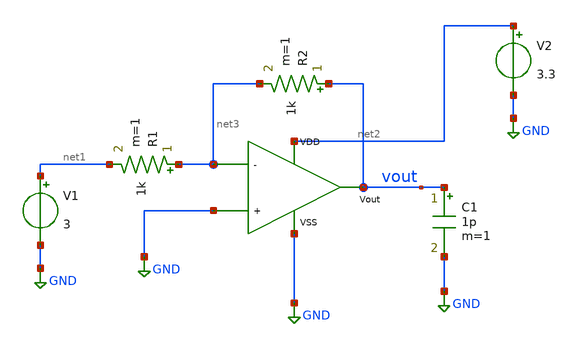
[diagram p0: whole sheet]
** sch_path: xschem/ota_miller/prueba.sch
**.subckt prueba
x1 net2 vout GND net3 GND ota_n_in
R1 net3 net1 1k m=1
R2 vout net3 1k m=1
V1 net1 GND 3
V2 net2 GND 3.3
C1 vout GND 1p m=1
**** begin user architecture code


.control
save all
* Coloracion de graficas
set color0=white
set color1=black
set color2=blue
set color3=red
set xbrushwidth=2

* 1. Convertir V1 a onda senoidal: Offset = 0V, Amplitud = 0.5V, Frecuencia = 1kHz
alter V1 sin(0 0.5 1k)

* 2. Simular 5 ms con paso de 1 us (5 ciclos de 1 kHz)
tran 1u 5m

* 3. Graficar la señal de salida Vout
plot v(Vout) title 'Respuesta Transitoria Inversor OTA 5T' xlabel 'Tiempo (s)' ylabel 'Voltaje (V)'
.endc




.include /home/ringosinye/eda/pdks/gf180mcuD/libs.tech/ngspice/design.ngspice
.lib /home/ringosinye/eda/pdks/gf180mcuD/libs.tech/ngspice/sm141064.ngspice typical
.param sw_stat_mismatch = 0


**** end user architecture code
**.ends

* expanding   symbol:  ota_n_in.sym # of pins=5
** sym_path: xschem/ota_miller/ota_n_in.sym
** sch_path: xschem/ota_miller/ota_n_in.sch
.subckt ota_n_in VDD Vout + - VSS
*.opin Vout
*.ipin VSS
*.ipin VDD
*.ipin +
*.ipin -
XM1 net2 + net1 VSS nfet_03v3 L=0.28u W=0.22u nf=1 ad='int((nf+1)/2) * W/nf * 0.18u' as='int((nf+2)/2) * W/nf * 0.18u'
+ pd='2*int((nf+1)/2) * (W/nf + 0.18u)' ps='2*int((nf+2)/2) * (W/nf + 0.18u)' nrd='0.18u / W' nrs='0.18u / W'
+ sa=0 sb=0 sd=0 m=1 par=1
XM2 Vout - net1 VSS nfet_03v3 L=0.28u W=0.22u nf=1 ad='int((nf+1)/2) * W/nf * 0.18u' as='int((nf+2)/2) * W/nf * 0.18u'
+ pd='2*int((nf+1)/2) * (W/nf + 0.18u)' ps='2*int((nf+2)/2) * (W/nf + 0.18u)' nrd='0.18u / W' nrs='0.18u / W'
+ sa=0 sb=0 sd=0 m=1 par=1
XM3 VDD VDD net2 VSS nfet_03v3 L=0.28u W=0.22u nf=1 ad='int((nf+1)/2) * W/nf * 0.18u' as='int((nf+2)/2) * W/nf * 0.18u'
+ pd='2*int((nf+1)/2) * (W/nf + 0.18u)' ps='2*int((nf+2)/2) * (W/nf + 0.18u)' nrd='0.18u / W' nrs='0.18u / W'
+ sa=0 sb=0 sd=0 m=1 par=1
XM4 VDD VDD Vout VSS nfet_03v3 L=0.28u W=0.22u nf=1 ad='int((nf+1)/2) * W/nf * 0.18u' as='int((nf+2)/2) * W/nf * 0.18u'
+ pd='2*int((nf+1)/2) * (W/nf + 0.18u)' ps='2*int((nf+2)/2) * (W/nf + 0.18u)' nrd='0.18u / W' nrs='0.18u / W'
+ sa=0 sb=0 sd=0 m=1 par=1
XM5 net1 net3 VSS VSS nfet_03v3 L=0.28u W=0.22u nf=1 ad='int((nf+1)/2) * W/nf * 0.18u' as='int((nf+2)/2) * W/nf * 0.18u'
+ pd='2*int((nf+1)/2) * (W/nf + 0.18u)' ps='2*int((nf+2)/2) * (W/nf + 0.18u)' nrd='0.18u / W' nrs='0.18u / W'
+ sa=0 sb=0 sd=0 m=1 par=1
XM6 net3 net3 VSS VSS nfet_03v3 L=0.28u W=0.22u nf=1 ad='int((nf+1)/2) * W/nf * 0.18u' as='int((nf+2)/2) * W/nf * 0.18u'
+ pd='2*int((nf+1)/2) * (W/nf + 0.18u)' ps='2*int((nf+2)/2) * (W/nf + 0.18u)' nrd='0.18u / W' nrs='0.18u / W'
+ sa=0 sb=0 sd=0 m=1 par=1
I0 VDD net3 1m
.ends

.GLOBAL GND
.end
